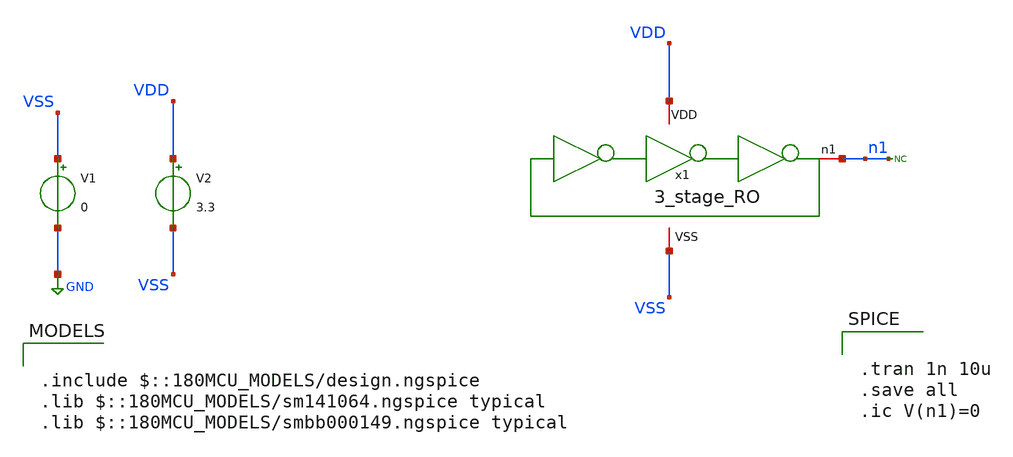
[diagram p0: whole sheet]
** sch_path: gf180_examples/RO/xschem/3_stage_RO_tb_tran.sch
**.subckt 3_stage_RO_tb_tran
x1 VDD VSS n1 3_stage_RO
V1 VSS GND 0
V2 VDD VSS 3.3
* noconn n1
**** begin user architecture code

.include $::180MCU_MODELS/design.ngspice
.lib $::180MCU_MODELS/sm141064.ngspice typical
.lib $::180MCU_MODELS/smbb000149.ngspice typical



.tran 1n 10u
.save all
.ic V(n1)=0


**** end user architecture code
**.ends
.GLOBAL GND
.end
